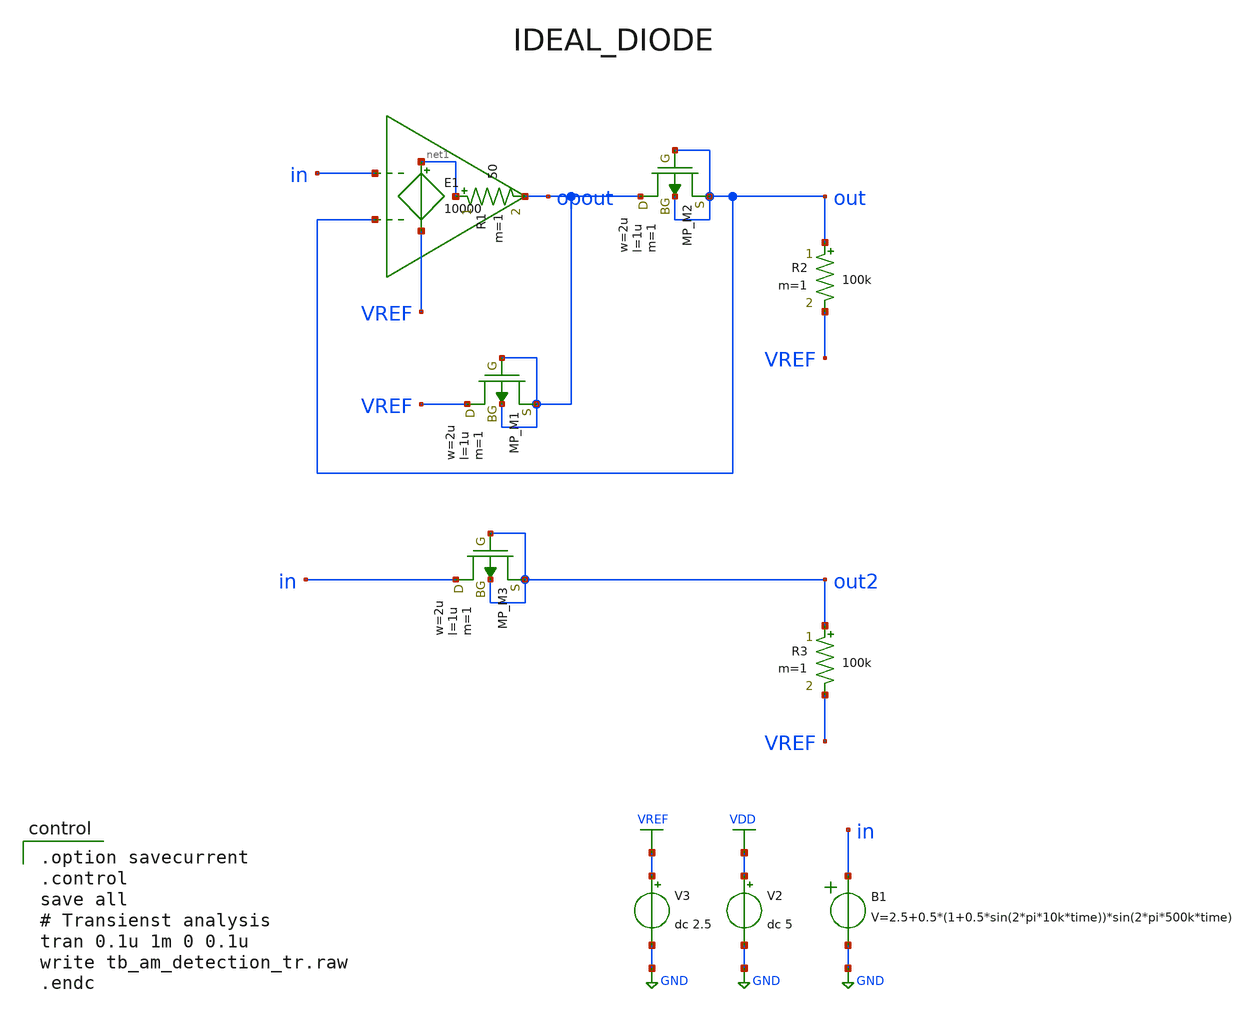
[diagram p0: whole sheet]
** sch_path: member_project/AM_Radio/Yamada3/xschem/tb_ideal_diode_orig.sch
**.subckt tb_ideal_diode_orig
V2 VDD GND dc 5
V3 VREF GND dc 2.5
B1 in GND V=2.5+0.5*(1+0.5*sin(2*pi*10k*time))*sin(2*pi*500k*time)
E1 net1 VREF in out 10000
XM1 VREF opout opout opout PMOS w=2u l=1u as=0 ad=0 ps=0 pd=0 nrd=0 nrs=0 m=1
XM2 opout out out out PMOS w=2u l=1u as=0 ad=0 ps=0 pd=0 nrd=0 nrs=0 m=1
R2 out VREF 100k m=1
XM3 in out2 out2 out2 PMOS w=2u l=1u as=0 ad=0 ps=0 pd=0 nrd=0 nrs=0 m=1
R3 out2 VREF 100k m=1
R1 net1 opout 50 m=1
**** begin user architecture code
 .include $::LIB/ip62_models

.option savecurrent
.control
save all
# Transienst analysis
tran 0.1u 1m 0 0.1u
write tb_am_detection_tr.raw
.endc

**** end user architecture code
**.ends
.GLOBAL GND
.GLOBAL VDD
.GLOBAL VREF
.end
